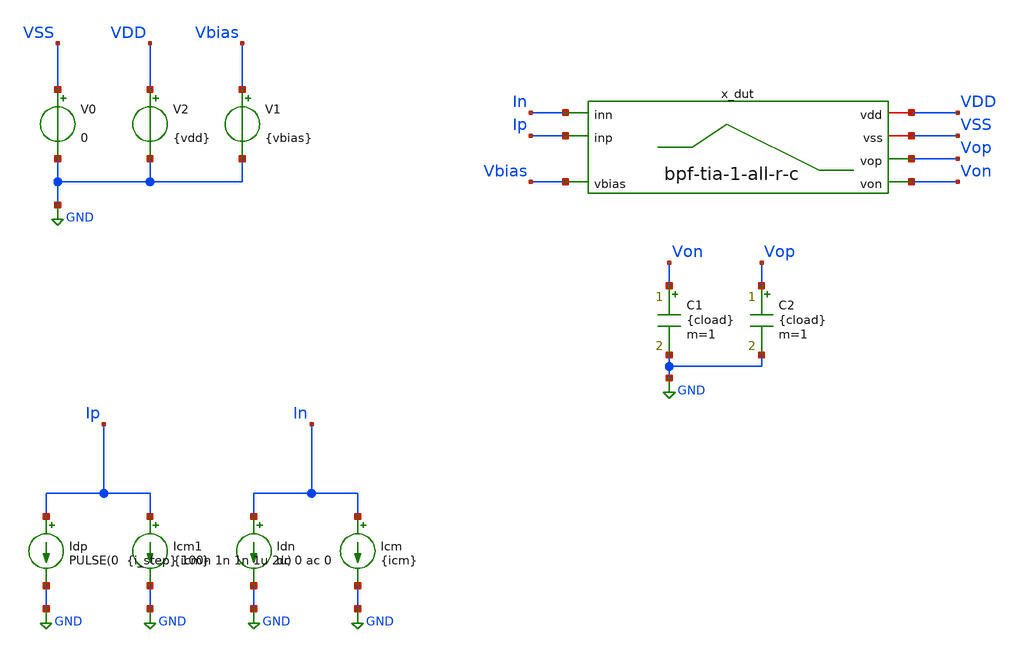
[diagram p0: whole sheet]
** sch_path: examples/tunable-tia/gf180/tia-bpf-1/tb_dc.sch
**.subckt tb_dc
V0 VSS GND 0
V2 VDD GND {vdd}
x_dut VDD VSS Vop Von In Ip Vbias bpf-tia-1-all-r-c
V1 Vbias GND {vbias}
C1 Von GND {cload} m=1
C2 Vop GND {cload} m=1
Icm In GND {icm}
Idn In GND dc 0 ac 0
Icm1 Ip GND {icm}
Idp Ip GND PULSE(0 {i_step} 100n 1n 1n 1u 2u)
**** begin user architecture code


.control

    echo ==================================
    echo start of Control
    echo ==================================

    save all

    echo
    echo (A) start of OP
    echo ----------------------------------

    * operating point
    op

    let gm_id_1_2 = @m.x_dut.xm1.m0[gm]/@m.x_dut.xm1.m0[id]

    print all
    write op.raw

    echo ----------------------------------
    echo END of OP
    echo ----------------------------------

    * set appendwrite
echo
    echo (B) start of DC Sweep
    echo ----------------------------------

    * example: sweep VIN from 0V to 1.8V in 0.01V steps
    *dc VIN 0 1.8 0.01

    * we sweep the differential current
    dc ICM 0 1.8u 0.01


    * post-processing
    let Vout_dc = v(Vop) - v(Von)

    * The following works if the DUT is voltage follower and configured in unity-gain
    *meas dc Vout_mid find Vout_dc when VIN=0.9
    *meas dc Vin_th when Vout_dc=0.9 cross=1
    plot Vout_dc vs ip

    echo ----------------------------------
    echo END of DC Sweep
    echo ----------------------------------

    echo
    echo (C) start of Transient Sim (step input)
    echo ----------------------------------

    * step input should be defined in netlist, e.g.:
    * VIN in 0 pulse(0 1.8 0 1n 1n 1u 2u)
    tran 1n 10u

    * post-processing
    let Vout_tran = v(Vop) - v(Von)
    meas tran t_delay trig v(Vin) val=0.9 rise=1 targ Vout_tran val=0.9 rise=1
    plot Vout_tran

    echo ----------------------------------
    echo END of Transient Step Sim
    echo ----------------------------------

    echo
    echo (D) start of Transient Sim (sinusoidal input)
    echo ----------------------------------

    * sinusoidal input should be defined in netlist, e.g.:
    * VIN in 0 sin(0 0.5 1e6 0 0)
    tran 1n 10u

    * post-processing
    let Vout_sin = v(Vop) - v(Von)
    fft Vout_sin
    plot Vout_sin

    echo ----------------------------------
    echo END of Transient Sin Sim
    echo ----------------------------------

    echo SAVING SIMULATION RESULTS IN THE RAW FILE
    save all
    write

    echo ==================================
    echo END of Control
    echo ==================================
.endc



.include $::180MCU_MODELS/design.ngspice
.lib $::180MCU_MODELS/sm141064.ngspice typical

.lib $::180MCU_MODELS/sm141064.ngspice res_typical
* .lib $::180MCU_MODELS/sm141064.ngspice res_statistical




*.option savecurrents
* Saving gm values for transistors
.save @m.x_dut.xm1.m0[gm]
.save @m.x_dut.xm2.m0[gm]

* Saving id values for transistors
.save @m.x_dut.xm1.m0[id]
.save @m.x_dut.xm2.m0[id]





.param icm=0.5e-6
.param i_step=0.5e-6

.param vdd=6.0
.param vbias=1.0

.param cload=1p





* All DUT parameters

* MOSFET PARAMETERS
.param x_dut_m1_2_w=0.22u
.param x_dut_m1_2_l=0.40u
.param x_dut_m1_2_nf=2

* PASSIVE ELEMENT PARAMETERS
.param x_dut_ldd=2n
.param x_dut_cdd=1n

.param x_dut_rs=1k

.param x_dut_r4=1k


**** end user architecture code
**.ends

* expanding   symbol:  tia-bpf-1/bpf-tia-1-all-r-c.sym # of pins=7
** sym_path: examples/tunable-tia/gf180/tia-bpf-1/bpf-tia-1-all-r-c.sym
** sch_path: examples/tunable-tia/gf180/tia-bpf-1/bpf-tia-1-all-r-c.sch
.subckt bpf-tia-1-all-r-c vdd vss vop von inn inp vbias
*.iopin vdd
*.iopin vss
*.ipin inp
*.ipin inn
*.opin von
*.opin vop
*.ipin vbias
XM1 von vbias inp vss nfet_03v3 L={x_dut_m1_2_l} W={x_dut_m1_2_w} nf=2 ad='int((nf+1)/2) * W/nf * 0.18u'
+ as='int((nf+2)/2) * W/nf * 0.18u' pd='2*int((nf+1)/2) * (W/nf + 0.18u)' ps='2*int((nf+2)/2) * (W/nf + 0.18u)'
+ nrd='0.18u / W' nrs='0.18u / W' sa=0 sb=0 sd=0 m=1
XM2 vop vbias inn vss nfet_03v3 L={x_dut_m1_2_l} W={x_dut_m1_2_w} nf=2 ad='int((nf+1)/2) * W/nf * 0.18u'
+ as='int((nf+2)/2) * W/nf * 0.18u' pd='2*int((nf+1)/2) * (W/nf + 0.18u)' ps='2*int((nf+2)/2) * (W/nf + 0.18u)'
+ nrd='0.18u / W' nrs='0.18u / W' sa=0 sb=0 sd=0 m=1
R1 inp vss {x_dut_rs} m=1
R2 inn vss {x_dut_rs} m=1
C1 vdd von {x_dut_cdd} m=1
C2 vdd vop {x_dut_cdd} m=1
L2 vdd von {x_dut_ldd} m=1
L3 vdd vop {x_dut_ldd} m=1
R4 von vop {x_dut_r4} m=1
.ends

.GLOBAL GND
.end
